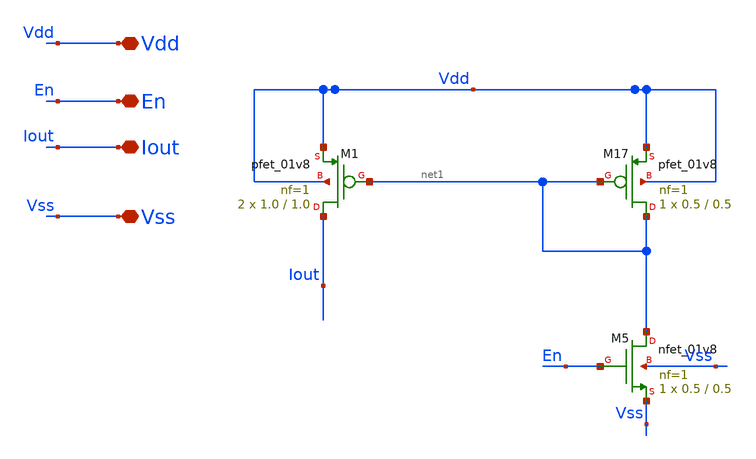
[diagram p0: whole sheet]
** sch_path: xschem/ref_gen_tt.sch
**.subckt ref_gen_tt Vdd En Iout Vss
*.iopin Vdd
*.iopin En
*.iopin Iout
*.iopin Vss
XM17 net1 net1 Vdd Vdd sky130_fd_pr__pfet_01v8 L=0.5 W=0.5 nf=1 ad='int((nf+1)/2) * W/nf * 0.29' as='int((nf+2)/2) * W/nf * 0.29'
+ pd='2*int((nf+1)/2) * (W/nf + 0.29)' ps='2*int((nf+2)/2) * (W/nf + 0.29)' nrd='0.29 / W' nrs='0.29 / W'
+ sa=0 sb=0 sd=0 mult=1 m=1
XM1 Iout net1 Vdd Vdd sky130_fd_pr__pfet_01v8 L=1.0 W=1.0 nf=1 ad='int((nf+1)/2) * W/nf * 0.29' as='int((nf+2)/2) * W/nf * 0.29'
+ pd='2*int((nf+1)/2) * (W/nf + 0.29)' ps='2*int((nf+2)/2) * (W/nf + 0.29)' nrd='0.29 / W' nrs='0.29 / W'
+ sa=0 sb=0 sd=0 mult=2 m=2
XM5 net1 En Vss Vss sky130_fd_pr__nfet_01v8 L=0.5 W=0.5 nf=1 ad='int((1 + 1)/2) * 0.5 / 1 * 0.29' as='int((1 + 2)/2) * 0.5 / 1 * 0.29'
+ pd='2*int((1 + 1)/2) * (0.5 / 1 + 0.29)' ps='2*int((1 + 2)/2) * (0.5 / 1 + 0.29)' nrd='0.29 / 0.5 ' nrs='0.29 / 0.5 '
+ sa=0 sb=0 sd=0 mult=1 m=1
**.ends
.end
